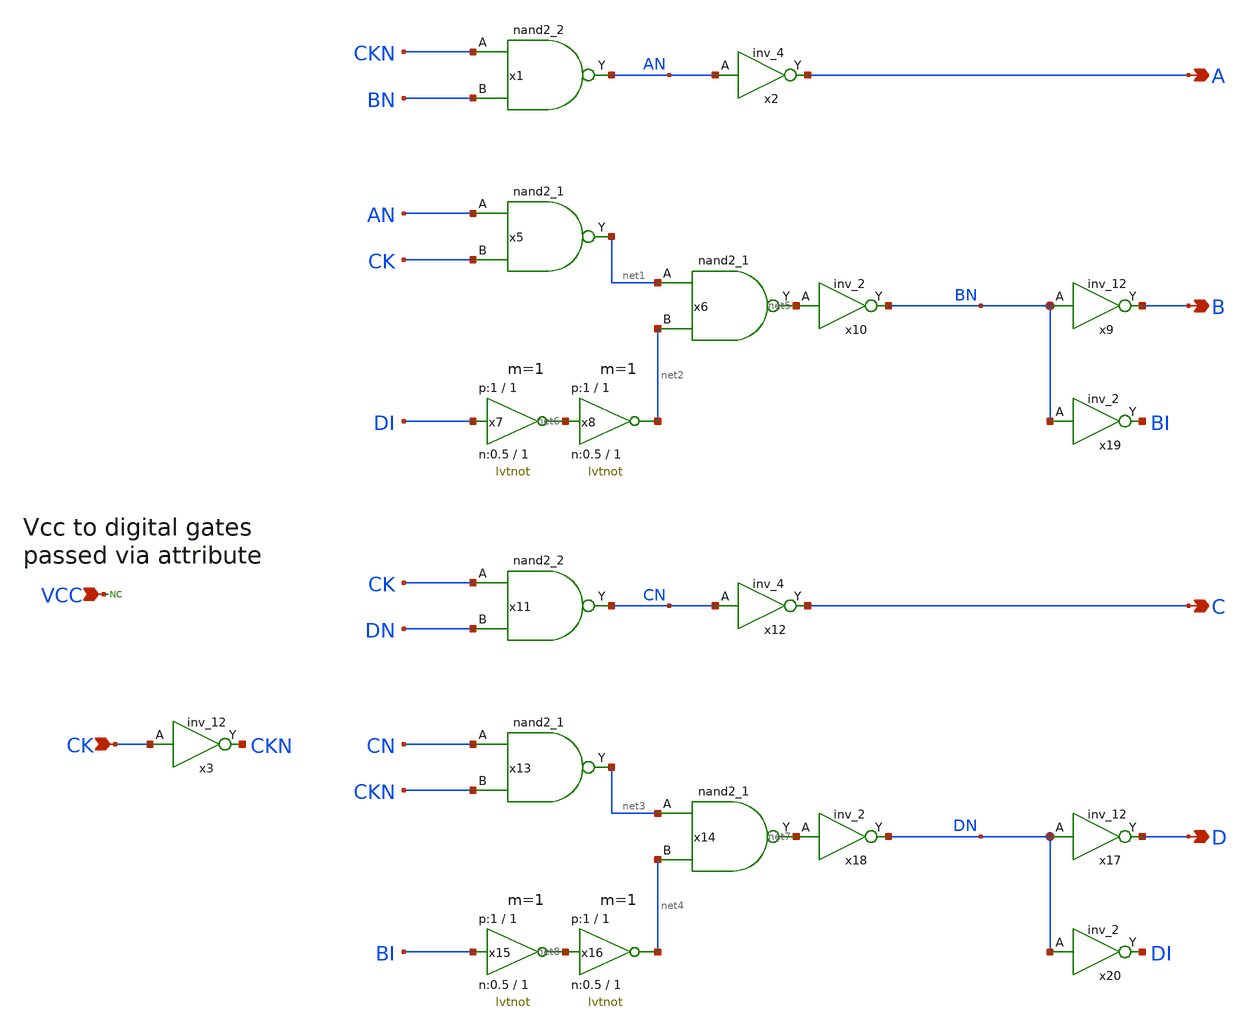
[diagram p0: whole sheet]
** sch_path: sky130A/xschem_libs/sky130_tests/charge_pump_phasegen/schematic/charge_pump_phasegen.sch
* Copyright 2021 Stefan Frederik Schippers
* Licensed under the Apache License, Version 2.0 (the "License");
* you may not use this file except in compliance with the License.
* You may obtain a copy of the License at
* https://www.apache.org/licenses/LICENSE-2.0
* Unless required by applicable law or agreed to in writing, software
* distributed under the License is distributed on an "AS IS" BASIS,
* WITHOUT WARRANTIES OR CONDITIONS OF ANY KIND, either express or implied.
* See the License for the specific language governing permissions and
* limitations under the License.
* StefanSchippers/xschem_sky130/sky130_tests/lvtnot.sch:
* Copyright 2020 Stefan Frederik Schippers
**.subckt charge_pump_phasegen CK A B C D VCC
*.ipin CK
*.opin A
*.opin B
*.opin C
*.opin D
*.ipin VCC
x1 CKN BN GND GND VCC VCC AN sky130_fd_sc_hd__nand2_2
x2 AN GND GND VCC VCC A sky130_fd_sc_hd__inv_4
x5 AN CK GND GND VCC VCC net1 sky130_fd_sc_hd__nand2_1
x6 net1 net2 GND GND VCC VCC net5 sky130_fd_sc_hd__nand2_1
x7 DI net6 VCC GND lvtnot W_N=0.5 L_N=1 W_P=1 L_P=1 m=1
x8 net6 net2 VCC GND lvtnot W_N=0.5 L_N=1 W_P=1 L_P=1 m=1
x9 BN GND GND VCC VCC B sky130_fd_sc_hd__inv_12
x10 net5 GND GND VCC VCC BN sky130_fd_sc_hd__inv_2
x11 CK DN GND GND VCC VCC CN sky130_fd_sc_hd__nand2_2
x12 CN GND GND VCC VCC C sky130_fd_sc_hd__inv_4
x13 CN CKN GND GND VCC VCC net3 sky130_fd_sc_hd__nand2_1
x14 net3 net4 GND GND VCC VCC net7 sky130_fd_sc_hd__nand2_1
x15 BI net8 VCC GND lvtnot W_N=0.5 L_N=1 W_P=1 L_P=1 m=1
x16 net8 net4 VCC GND lvtnot W_N=0.5 L_N=1 W_P=1 L_P=1 m=1
x17 DN GND GND VCC VCC D sky130_fd_sc_hd__inv_12
x18 net7 GND GND VCC VCC DN sky130_fd_sc_hd__inv_2
x3 CK GND GND VCC VCC CKN sky130_fd_sc_hd__inv_12
* noconn VCC
x19 BN GND GND VCC VCC BI sky130_fd_sc_hd__inv_2
x20 DN GND GND VCC VCC DI sky130_fd_sc_hd__inv_2
**.ends

* expanding   symbol:  sky130_tests/lvtnot.sym # of pins=2
** sym_path: sky130_tests/lvtnot.sym
** sch_path: sky130_tests/lvtnot.sch
.subckt lvtnot a y VCCPIN VSSPIN     W_N=1 L_N=0.15 W_P=2 L_P=0.35
*.opin y
*.ipin a
XM1 y a VSSPIN VSSPIN sky130_fd_pr__nfet_01v8_lvt L=L_N W=W_N nf=1 ad='int((1 + 1)/2) * W_N / 1 * 0.29'
+ as='int((1 + 2)/2) * W_N / 1 * 0.29' pd='2*int((1 + 1)/2) * (W_N / 1 + 0.29)' ps='2*int((1 + 2)/2) * (W_N / 1 + 0.29)'
+ nrd='0.29 / W_N ' nrs='0.29 / W_N ' sa=0 sb=0 sd=0 mult=1 m=1
XM2 y a VCCPIN VCCPIN sky130_fd_pr__pfet_01v8_lvt L=L_P W=W_P nf=1 ad='int((1 + 1)/2) * W_P / 1 * 0.29'
+ as='int((1 + 2)/2) * W_P / 1 * 0.29' pd='2*int((1 + 1)/2) * (W_P / 1 + 0.29)' ps='2*int((1 + 2)/2) * (W_P / 1 + 0.29)'
+ nrd='0.29 / W_P ' nrs='0.29 / W_P ' sa=0 sb=0 sd=0 mult=1 m=1
.ends

.end
